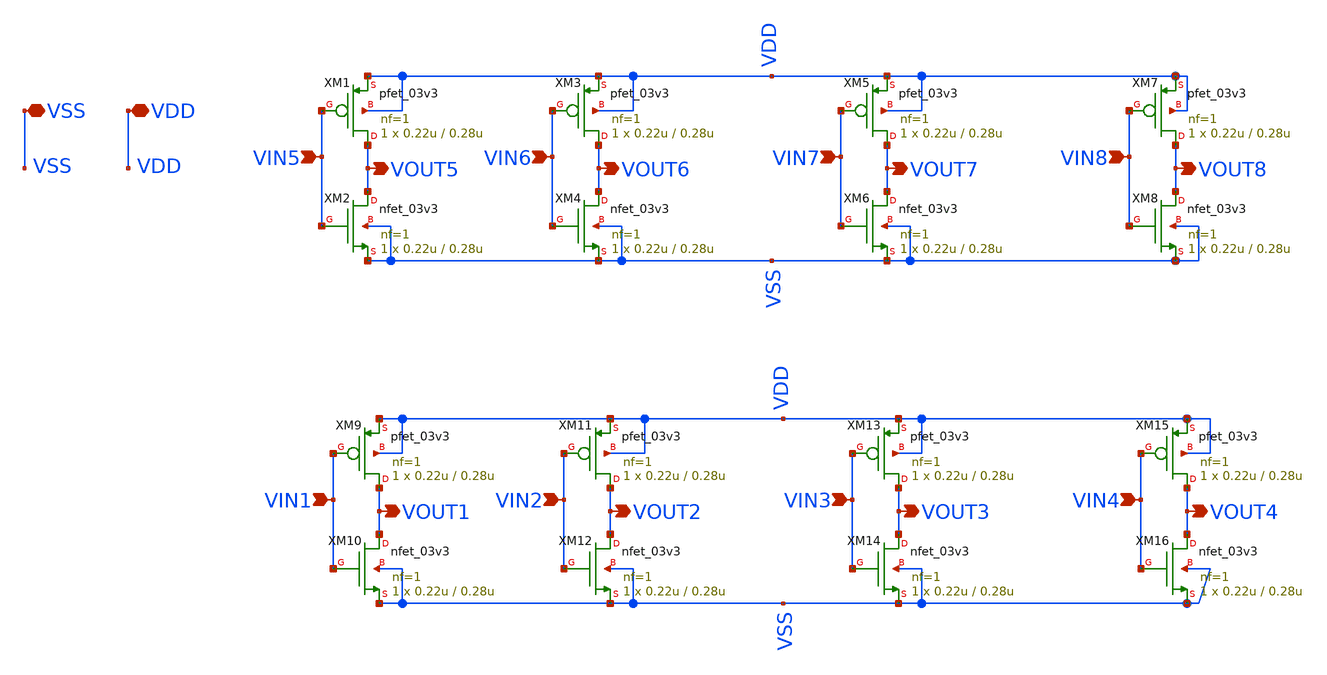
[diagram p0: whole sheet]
** sch_path: analog/top/inverter_block.sch
**.subckt inverter_block VIN1 VIN2 VIN3 VIN4 VIN5 VIN6 VIN7 VIN8 VOUT1 VOUT2 VOUT3 VOUT4 VOUT5 VOUT6
*+ VOUT7 VOUT8 VDD VSS
*.ipin VIN1
*.ipin VIN2
*.ipin VIN3
*.ipin VIN4
*.ipin VIN5
*.ipin VIN6
*.ipin VIN7
*.ipin VIN8
*.opin VOUT1
*.opin VOUT2
*.opin VOUT3
*.opin VOUT4
*.opin VOUT5
*.opin VOUT6
*.opin VOUT7
*.opin VOUT8
*.iopin VDD
*.iopin VSS
XM9 VOUT1 VIN1 VDD VDD pfet_03v3 L=0.28u W=0.22u nf=1 ad='int((nf+1)/2) * W/nf * 0.18u' as='int((nf+2)/2) * W/nf * 0.18u'
+ pd='2*int((nf+1)/2) * (W/nf + 0.18u)' ps='2*int((nf+2)/2) * (W/nf + 0.18u)' nrd='0.18u / W' nrs='0.18u / W'
+ sa=0 sb=0 sd=0 m=1
XM10 VOUT1 VIN1 VSS VSS nfet_03v3 L=0.28u W=0.22u nf=1 ad='int((nf+1)/2) * W/nf * 0.18u' as='int((nf+2)/2) * W/nf * 0.18u'
+ pd='2*int((nf+1)/2) * (W/nf + 0.18u)' ps='2*int((nf+2)/2) * (W/nf + 0.18u)' nrd='0.18u / W' nrs='0.18u / W'
+ sa=0 sb=0 sd=0 m=1
XM11 VOUT2 VIN2 VDD VDD pfet_03v3 L=0.28u W=0.22u nf=1 ad='int((nf+1)/2) * W/nf * 0.18u' as='int((nf+2)/2) * W/nf * 0.18u'
+ pd='2*int((nf+1)/2) * (W/nf + 0.18u)' ps='2*int((nf+2)/2) * (W/nf + 0.18u)' nrd='0.18u / W' nrs='0.18u / W'
+ sa=0 sb=0 sd=0 m=1
XM12 VOUT2 VIN2 VSS VSS nfet_03v3 L=0.28u W=0.22u nf=1 ad='int((nf+1)/2) * W/nf * 0.18u' as='int((nf+2)/2) * W/nf * 0.18u'
+ pd='2*int((nf+1)/2) * (W/nf + 0.18u)' ps='2*int((nf+2)/2) * (W/nf + 0.18u)' nrd='0.18u / W' nrs='0.18u / W'
+ sa=0 sb=0 sd=0 m=1
XM13 VOUT3 VIN3 VDD VDD pfet_03v3 L=0.28u W=0.22u nf=1 ad='int((nf+1)/2) * W/nf * 0.18u' as='int((nf+2)/2) * W/nf * 0.18u'
+ pd='2*int((nf+1)/2) * (W/nf + 0.18u)' ps='2*int((nf+2)/2) * (W/nf + 0.18u)' nrd='0.18u / W' nrs='0.18u / W'
+ sa=0 sb=0 sd=0 m=1
XM14 VOUT3 VIN3 VSS VSS nfet_03v3 L=0.28u W=0.22u nf=1 ad='int((nf+1)/2) * W/nf * 0.18u' as='int((nf+2)/2) * W/nf * 0.18u'
+ pd='2*int((nf+1)/2) * (W/nf + 0.18u)' ps='2*int((nf+2)/2) * (W/nf + 0.18u)' nrd='0.18u / W' nrs='0.18u / W'
+ sa=0 sb=0 sd=0 m=1
XM15 VOUT4 VIN4 VDD VDD pfet_03v3 L=0.28u W=0.22u nf=1 ad='int((nf+1)/2) * W/nf * 0.18u' as='int((nf+2)/2) * W/nf * 0.18u'
+ pd='2*int((nf+1)/2) * (W/nf + 0.18u)' ps='2*int((nf+2)/2) * (W/nf + 0.18u)' nrd='0.18u / W' nrs='0.18u / W'
+ sa=0 sb=0 sd=0 m=1
XM16 VOUT4 VIN4 VSS VSS nfet_03v3 L=0.28u W=0.22u nf=1 ad='int((nf+1)/2) * W/nf * 0.18u' as='int((nf+2)/2) * W/nf * 0.18u'
+ pd='2*int((nf+1)/2) * (W/nf + 0.18u)' ps='2*int((nf+2)/2) * (W/nf + 0.18u)' nrd='0.18u / W' nrs='0.18u / W'
+ sa=0 sb=0 sd=0 m=1
XM1 VOUT5 VIN5 VDD VDD pfet_03v3 L=0.28u W=0.22u nf=1 ad='int((nf+1)/2) * W/nf * 0.18u' as='int((nf+2)/2) * W/nf * 0.18u'
+ pd='2*int((nf+1)/2) * (W/nf + 0.18u)' ps='2*int((nf+2)/2) * (W/nf + 0.18u)' nrd='0.18u / W' nrs='0.18u / W'
+ sa=0 sb=0 sd=0 m=1
XM2 VOUT5 VIN5 VSS VSS nfet_03v3 L=0.28u W=0.22u nf=1 ad='int((nf+1)/2) * W/nf * 0.18u' as='int((nf+2)/2) * W/nf * 0.18u'
+ pd='2*int((nf+1)/2) * (W/nf + 0.18u)' ps='2*int((nf+2)/2) * (W/nf + 0.18u)' nrd='0.18u / W' nrs='0.18u / W'
+ sa=0 sb=0 sd=0 m=1
XM3 VOUT6 VIN6 VDD VDD pfet_03v3 L=0.28u W=0.22u nf=1 ad='int((nf+1)/2) * W/nf * 0.18u' as='int((nf+2)/2) * W/nf * 0.18u'
+ pd='2*int((nf+1)/2) * (W/nf + 0.18u)' ps='2*int((nf+2)/2) * (W/nf + 0.18u)' nrd='0.18u / W' nrs='0.18u / W'
+ sa=0 sb=0 sd=0 m=1
XM4 VOUT6 VIN6 VSS VSS nfet_03v3 L=0.28u W=0.22u nf=1 ad='int((nf+1)/2) * W/nf * 0.18u' as='int((nf+2)/2) * W/nf * 0.18u'
+ pd='2*int((nf+1)/2) * (W/nf + 0.18u)' ps='2*int((nf+2)/2) * (W/nf + 0.18u)' nrd='0.18u / W' nrs='0.18u / W'
+ sa=0 sb=0 sd=0 m=1
XM5 VOUT7 VIN7 VDD VDD pfet_03v3 L=0.28u W=0.22u nf=1 ad='int((nf+1)/2) * W/nf * 0.18u' as='int((nf+2)/2) * W/nf * 0.18u'
+ pd='2*int((nf+1)/2) * (W/nf + 0.18u)' ps='2*int((nf+2)/2) * (W/nf + 0.18u)' nrd='0.18u / W' nrs='0.18u / W'
+ sa=0 sb=0 sd=0 m=1
XM6 VOUT7 VIN7 VSS VSS nfet_03v3 L=0.28u W=0.22u nf=1 ad='int((nf+1)/2) * W/nf * 0.18u' as='int((nf+2)/2) * W/nf * 0.18u'
+ pd='2*int((nf+1)/2) * (W/nf + 0.18u)' ps='2*int((nf+2)/2) * (W/nf + 0.18u)' nrd='0.18u / W' nrs='0.18u / W'
+ sa=0 sb=0 sd=0 m=1
XM7 VOUT8 VIN8 VDD VDD pfet_03v3 L=0.28u W=0.22u nf=1 ad='int((nf+1)/2) * W/nf * 0.18u' as='int((nf+2)/2) * W/nf * 0.18u'
+ pd='2*int((nf+1)/2) * (W/nf + 0.18u)' ps='2*int((nf+2)/2) * (W/nf + 0.18u)' nrd='0.18u / W' nrs='0.18u / W'
+ sa=0 sb=0 sd=0 m=1
XM8 VOUT8 VIN8 VSS VSS nfet_03v3 L=0.28u W=0.22u nf=1 ad='int((nf+1)/2) * W/nf * 0.18u' as='int((nf+2)/2) * W/nf * 0.18u'
+ pd='2*int((nf+1)/2) * (W/nf + 0.18u)' ps='2*int((nf+2)/2) * (W/nf + 0.18u)' nrd='0.18u / W' nrs='0.18u / W'
+ sa=0 sb=0 sd=0 m=1
**.ends
.end
